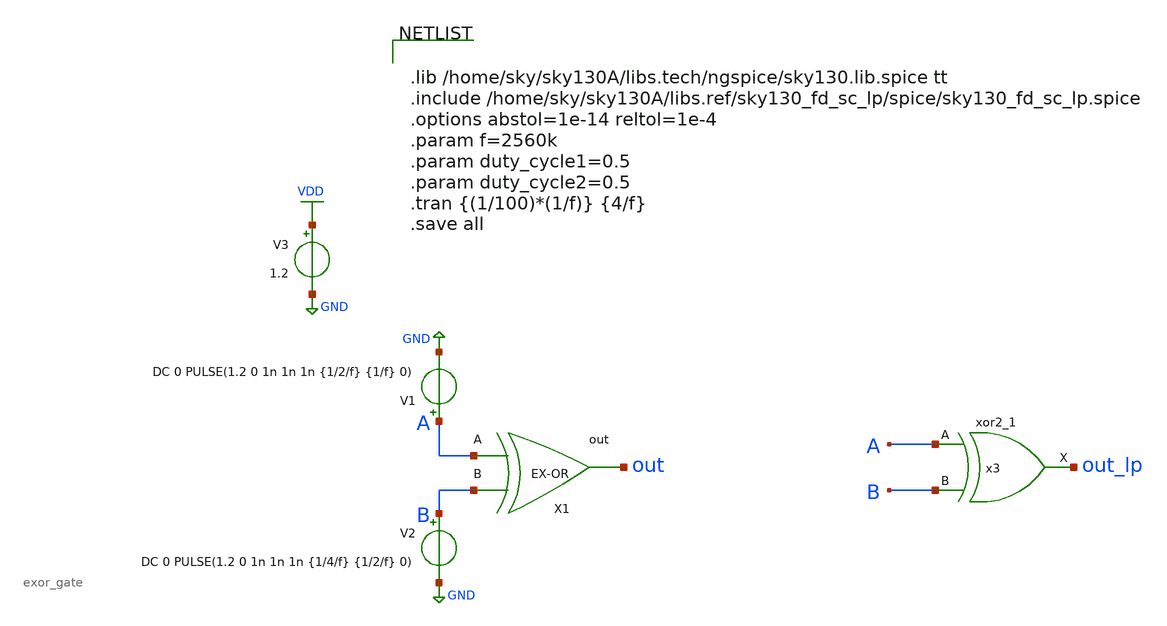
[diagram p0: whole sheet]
** sch_path: xschem/exor_gate/exor_gate_tb.sch
**.subckt exor_gate_tb
X1 A B out exor_gate
V1 A GND DC 0 PULSE(1.2 0 1n 1n 1n {1/2/f} {1/f} 0)
V2 B GND DC 0 PULSE(1.2 0 1n 1n 1n {1/4/f} {1/2/f} 0)
V3 VDD GND 1.2
x3 A B GND GND VDD VDD out_lp sky130_fd_sc_lp__xor2_1
**** begin user architecture code


.lib /home/sky/sky130A/libs.tech/ngspice/sky130.lib.spice tt
.include /home/sky/sky130A/libs.ref/sky130_fd_sc_lp/spice/sky130_fd_sc_lp.spice
.options abstol=1e-14 reltol=1e-4
.param f=2560k
.param duty_cycle1=0.5
.param duty_cycle2=0.5
.tran {(1/100)*(1/f)} {4/f}
.save all


**** end user architecture code
**.ends

* expanding   symbol:  exor_gate/exor_gate.sym # of pins=3
** sym_path: xschem/exor_gate/exor_gate.sym
** sch_path: xschem/exor_gate/exor_gate.sch
.subckt exor_gate A B out
*.ipin A
*.ipin B
*.opin out
XM4 out A net1 GND sky130_fd_pr__nfet_01v8 L=0.18 W=0.5 nf=1 ad='int((nf+1)/2) * W/nf * 0.29' as='int((nf+2)/2) * W/nf * 0.29'
+ pd='2*int((nf+1)/2) * (W/nf + 0.29)' ps='2*int((nf+2)/2) * (W/nf + 0.29)' nrd='0.29 / W' nrs='0.29 / W'
+ sa=0 sb=0 sd=0 mult=1 m=1
XM5 net3 B VDD VDD sky130_fd_pr__pfet_01v8 L=0.18 W=1 nf=1 ad='int((nf+1)/2) * W/nf * 0.29' as='int((nf+2)/2) * W/nf * 0.29'
+ pd='2*int((nf+1)/2) * (W/nf + 0.29)' ps='2*int((nf+2)/2) * (W/nf + 0.29)' nrd='0.29 / W' nrs='0.29 / W'
+ sa=0 sb=0 sd=0 mult=1 m=1
XM1 net1 B GND GND sky130_fd_pr__nfet_01v8 L=0.18 W=0.5 nf=1 ad='int((nf+1)/2) * W/nf * 0.29' as='int((nf+2)/2) * W/nf * 0.29'
+ pd='2*int((nf+1)/2) * (W/nf + 0.29)' ps='2*int((nf+2)/2) * (W/nf + 0.29)' nrd='0.29 / W' nrs='0.29 / W'
+ sa=0 sb=0 sd=0 mult=1 m=1
XM2 out net5 net3 VDD sky130_fd_pr__pfet_01v8 L=0.18 W=1 nf=1 ad='int((nf+1)/2) * W/nf * 0.29' as='int((nf+2)/2) * W/nf * 0.29'
+ pd='2*int((nf+1)/2) * (W/nf + 0.29)' ps='2*int((nf+2)/2) * (W/nf + 0.29)' nrd='0.29 / W' nrs='0.29 / W'
+ sa=0 sb=0 sd=0 mult=1 m=1
XM3 net4 net6 VDD VDD sky130_fd_pr__pfet_01v8 L=0.18 W=1 nf=1 ad='int((nf+1)/2) * W/nf * 0.29' as='int((nf+2)/2) * W/nf * 0.29'
+ pd='2*int((nf+1)/2) * (W/nf + 0.29)' ps='2*int((nf+2)/2) * (W/nf + 0.29)' nrd='0.29 / W' nrs='0.29 / W'
+ sa=0 sb=0 sd=0 mult=1 m=1
XM6 out A net4 VDD sky130_fd_pr__pfet_01v8 L=0.18 W=1 nf=1 ad='int((nf+1)/2) * W/nf * 0.29' as='int((nf+2)/2) * W/nf * 0.29'
+ pd='2*int((nf+1)/2) * (W/nf + 0.29)' ps='2*int((nf+2)/2) * (W/nf + 0.29)' nrd='0.29 / W' nrs='0.29 / W'
+ sa=0 sb=0 sd=0 mult=1 m=1
XM7 out net5 net2 GND sky130_fd_pr__nfet_01v8 L=0.18 W=0.5 nf=1 ad='int((nf+1)/2) * W/nf * 0.29' as='int((nf+2)/2) * W/nf * 0.29'
+ pd='2*int((nf+1)/2) * (W/nf + 0.29)' ps='2*int((nf+2)/2) * (W/nf + 0.29)' nrd='0.29 / W' nrs='0.29 / W'
+ sa=0 sb=0 sd=0 mult=1 m=1
XM8 net2 net6 GND GND sky130_fd_pr__nfet_01v8 L=0.18 W=0.5 nf=1 ad='int((nf+1)/2) * W/nf * 0.29' as='int((nf+2)/2) * W/nf * 0.29'
+ pd='2*int((nf+1)/2) * (W/nf + 0.29)' ps='2*int((nf+2)/2) * (W/nf + 0.29)' nrd='0.29 / W' nrs='0.29 / W'
+ sa=0 sb=0 sd=0 mult=1 m=1
X3 B net6 inv Wpmos=3 Lpmos=0.18 Wnmos=1 Lnmos=0.18
X2 A net5 inv Wpmos=3 Lpmos=0.18 Wnmos=1 Lnmos=0.18
.ends


* expanding   symbol:  inv/inv.sym # of pins=2
** sym_path: xschem/inv/inv.sym
** sch_path: xschem/inv/inv.sch
.subckt inv in out  Wpmos=3 Lpmos=0.18 Wnmos=1 Lnmos=0.18
*.ipin in
*.iopin out
XM1 out in GND GND sky130_fd_pr__nfet_01v8 L=Lnmos W=Wnmos nf=1 ad='int((nf+1)/2) * W/nf * 0.29' as='int((nf+2)/2) * W/nf * 0.29'
+ pd='2*int((nf+1)/2) * (W/nf + 0.29)' ps='2*int((nf+2)/2) * (W/nf + 0.29)' nrd='0.29 / W' nrs='0.29 / W'
+ sa=0 sb=0 sd=0 mult=1 m=1
XM2 out in VDD VDD sky130_fd_pr__pfet_01v8 L=Lpmos W=Wpmos nf=1 ad='int((nf+1)/2) * W/nf * 0.29' as='int((nf+2)/2) * W/nf * 0.29'
+ pd='2*int((nf+1)/2) * (W/nf + 0.29)' ps='2*int((nf+2)/2) * (W/nf + 0.29)' nrd='0.29 / W' nrs='0.29 / W'
+ sa=0 sb=0 sd=0 mult=1 m=1
.ends

.GLOBAL GND
.GLOBAL VDD
.end
